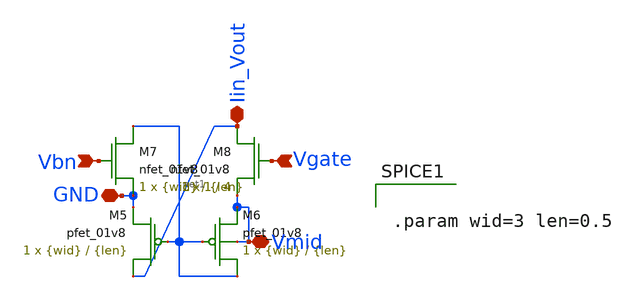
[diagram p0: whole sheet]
** sch_path: final/LDS/IV_converter_LDS.sch
**.subckt IV_converter_LDS Iin_Vout GND Vmid Vbn Vgate
*.iopin Iin_Vout
*.iopin GND
*.iopin Vmid
*.ipin Vbn
*.ipin Vgate
XM5 Iin_Vout net1 GND VDD sky130_fd_pr__pfet_01v8 L={len} W={wid} nf=1 ad='int((nf+1)/2) * W/nf * 0.29'
+ as='int((nf+2)/2) * W/nf * 0.29' pd='2*int((nf+1)/2) * (W/nf + 0.29)' ps='2*int((nf+2)/2) * (W/nf + 0.29)'
+ nrd='0.29 / W' nrs='0.29 / W' sa=0 sb=0 sd=0 mult=1 m=1
XM6 net1 net1 Vmid Vmid sky130_fd_pr__pfet_01v8 L={len} W={wid} nf=1 ad='int((nf+1)/2) * W/nf * 0.29'
+ as='int((nf+2)/2) * W/nf * 0.29' pd='2*int((nf+1)/2) * (W/nf + 0.29)' ps='2*int((nf+2)/2) * (W/nf + 0.29)'
+ nrd='0.29 / W' nrs='0.29 / W' sa=0 sb=0 sd=0 mult=1 m=1
XM7 net1 Vbn GND GND sky130_fd_pr__nfet_01v8 L={len} W={wid} nf=1 ad='int((nf+1)/2) * W/nf * 0.29' as='int((nf+2)/2) * W/nf * 0.29'
+ pd='2*int((nf+1)/2) * (W/nf + 0.29)' ps='2*int((nf+2)/2) * (W/nf + 0.29)' nrd='0.29 / W' nrs='0.29 / W'
+ sa=0 sb=0 sd=0 mult=1 m=1
XM8 Iin_Vout Vgate Vmid GND sky130_fd_pr__nfet_01v8 L=4 W=1 nf=1 ad='int((nf+1)/2) * W/nf * 0.29' as='int((nf+2)/2) * W/nf * 0.29'
+ pd='2*int((nf+1)/2) * (W/nf + 0.29)' ps='2*int((nf+2)/2) * (W/nf + 0.29)' nrd='0.29 / W' nrs='0.29 / W'
+ sa=0 sb=0 sd=0 mult=1 m=1
**** begin user architecture code


.param wid=3 len=0.5


**** end user architecture code
**.ends
.end
